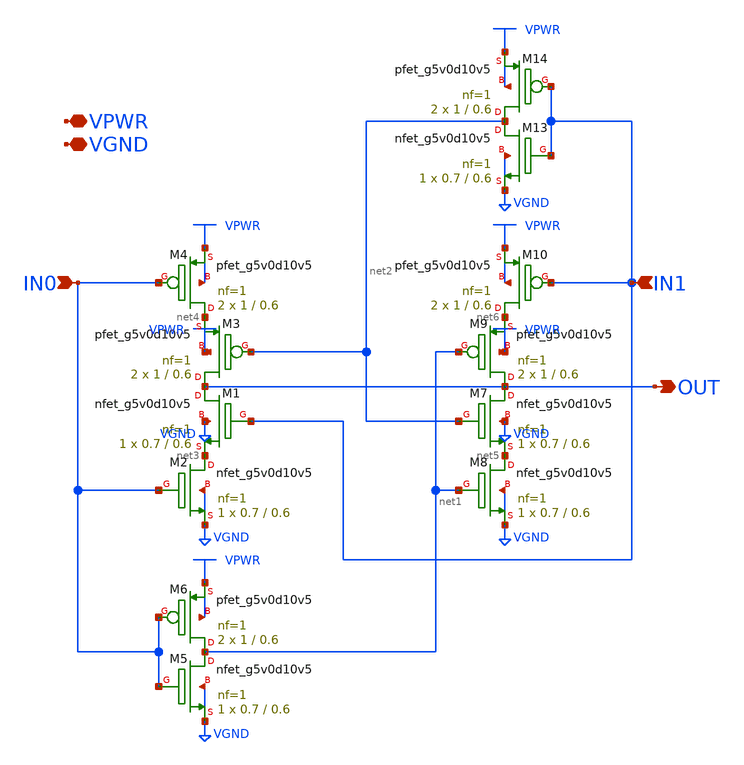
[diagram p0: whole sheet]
** sch_path: common/hvsbt_xor.sch
* Copyright 2023 David Mitchell Bailey
* Licensed under the Apache License, Version 2.0 (the "License");
* you may not use this file except in compliance with the License.
* You may obtain a copy of the License at
* https://www.apache.org/licenses/LICENSE-2.0
* Unless required by applicable law or agreed to in writing, software
* distributed under the License is distributed on an "AS IS" BASIS,
* WITHOUT WARRANTIES OR CONDITIONS OF ANY KIND, either express or implied.
* See the License for the specific language governing permissions and
* limitations under the License.
**.subckt hvsbt_xor IN0 VPWR VGND IN1 OUT
*.ipin IN0
*.iopin VPWR
*.iopin VGND
*.ipin IN1
*.opin OUT
XM1 OUT IN1 net3 VGND sky130_fd_pr__nfet_g5v0d10v5 L=0.6 W=0.7 nf=1 ad='int((nf+1)/2) * W/nf * 0.29'
+ as='int((nf+2)/2) * W/nf * 0.29' pd='2*int((nf+1)/2) * (W/nf + 0.29)' ps='2*int((nf+2)/2) * (W/nf + 0.29)'
+ nrd='0.29 / W' nrs='0.29 / W' sa=0 sb=0 sd=0 mult=1 m=1
XM2 net3 IN0 VGND VGND sky130_fd_pr__nfet_g5v0d10v5 L=0.6 W=0.7 nf=1 ad='int((nf+1)/2) * W/nf * 0.29'
+ as='int((nf+2)/2) * W/nf * 0.29' pd='2*int((nf+1)/2) * (W/nf + 0.29)' ps='2*int((nf+2)/2) * (W/nf + 0.29)'
+ nrd='0.29 / W' nrs='0.29 / W' sa=0 sb=0 sd=0 mult=1 m=1
XM3 OUT net2 net4 VPWR sky130_fd_pr__pfet_g5v0d10v5 L=0.6 W=1 nf=1 ad='int((nf+1)/2) * W/nf * 0.29' as='int((nf+2)/2) * W/nf * 0.29'
+ pd='2*int((nf+1)/2) * (W/nf + 0.29)' ps='2*int((nf+2)/2) * (W/nf + 0.29)' nrd='0.29 / W' nrs='0.29 / W'
+ sa=0 sb=0 sd=0 mult=2 m=2
XM4 net4 IN0 VPWR VPWR sky130_fd_pr__pfet_g5v0d10v5 L=0.6 W=1 nf=1 ad='int((nf+1)/2) * W/nf * 0.29' as='int((nf+2)/2) * W/nf * 0.29'
+ pd='2*int((nf+1)/2) * (W/nf + 0.29)' ps='2*int((nf+2)/2) * (W/nf + 0.29)' nrd='0.29 / W' nrs='0.29 / W'
+ sa=0 sb=0 sd=0 mult=2 m=2
XM5 net1 IN0 VGND VGND sky130_fd_pr__nfet_g5v0d10v5 L=0.6 W=0.7 nf=1 ad='int((nf+1)/2) * W/nf * 0.29'
+ as='int((nf+2)/2) * W/nf * 0.29' pd='2*int((nf+1)/2) * (W/nf + 0.29)' ps='2*int((nf+2)/2) * (W/nf + 0.29)'
+ nrd='0.29 / W' nrs='0.29 / W' sa=0 sb=0 sd=0 mult=1 m=1
XM6 net1 IN0 VPWR VPWR sky130_fd_pr__pfet_g5v0d10v5 L=0.6 W=1 nf=1 ad='int((nf+1)/2) * W/nf * 0.29' as='int((nf+2)/2) * W/nf * 0.29'
+ pd='2*int((nf+1)/2) * (W/nf + 0.29)' ps='2*int((nf+2)/2) * (W/nf + 0.29)' nrd='0.29 / W' nrs='0.29 / W'
+ sa=0 sb=0 sd=0 mult=2 m=2
XM7 OUT net2 net5 VGND sky130_fd_pr__nfet_g5v0d10v5 L=0.6 W=0.7 nf=1 ad='int((nf+1)/2) * W/nf * 0.29'
+ as='int((nf+2)/2) * W/nf * 0.29' pd='2*int((nf+1)/2) * (W/nf + 0.29)' ps='2*int((nf+2)/2) * (W/nf + 0.29)'
+ nrd='0.29 / W' nrs='0.29 / W' sa=0 sb=0 sd=0 mult=1 m=1
XM8 net5 net1 VGND VGND sky130_fd_pr__nfet_g5v0d10v5 L=0.6 W=0.7 nf=1 ad='int((nf+1)/2) * W/nf * 0.29'
+ as='int((nf+2)/2) * W/nf * 0.29' pd='2*int((nf+1)/2) * (W/nf + 0.29)' ps='2*int((nf+2)/2) * (W/nf + 0.29)'
+ nrd='0.29 / W' nrs='0.29 / W' sa=0 sb=0 sd=0 mult=1 m=1
XM9 OUT net1 net6 VPWR sky130_fd_pr__pfet_g5v0d10v5 L=0.6 W=1 nf=1 ad='int((nf+1)/2) * W/nf * 0.29' as='int((nf+2)/2) * W/nf * 0.29'
+ pd='2*int((nf+1)/2) * (W/nf + 0.29)' ps='2*int((nf+2)/2) * (W/nf + 0.29)' nrd='0.29 / W' nrs='0.29 / W'
+ sa=0 sb=0 sd=0 mult=2 m=2
XM10 net6 IN1 VPWR VPWR sky130_fd_pr__pfet_g5v0d10v5 L=0.6 W=1 nf=1 ad='int((nf+1)/2) * W/nf * 0.29'
+ as='int((nf+2)/2) * W/nf * 0.29' pd='2*int((nf+1)/2) * (W/nf + 0.29)' ps='2*int((nf+2)/2) * (W/nf + 0.29)'
+ nrd='0.29 / W' nrs='0.29 / W' sa=0 sb=0 sd=0 mult=2 m=2
XM13 net2 IN1 VGND VGND sky130_fd_pr__nfet_g5v0d10v5 L=0.6 W=0.7 nf=1 ad='int((nf+1)/2) * W/nf * 0.29'
+ as='int((nf+2)/2) * W/nf * 0.29' pd='2*int((nf+1)/2) * (W/nf + 0.29)' ps='2*int((nf+2)/2) * (W/nf + 0.29)'
+ nrd='0.29 / W' nrs='0.29 / W' sa=0 sb=0 sd=0 mult=1 m=1
XM14 net2 IN1 VPWR VPWR sky130_fd_pr__pfet_g5v0d10v5 L=0.6 W=1 nf=1 ad='int((nf+1)/2) * W/nf * 0.29'
+ as='int((nf+2)/2) * W/nf * 0.29' pd='2*int((nf+1)/2) * (W/nf + 0.29)' ps='2*int((nf+2)/2) * (W/nf + 0.29)'
+ nrd='0.29 / W' nrs='0.29 / W' sa=0 sb=0 sd=0 mult=2 m=2
**.ends
.end
